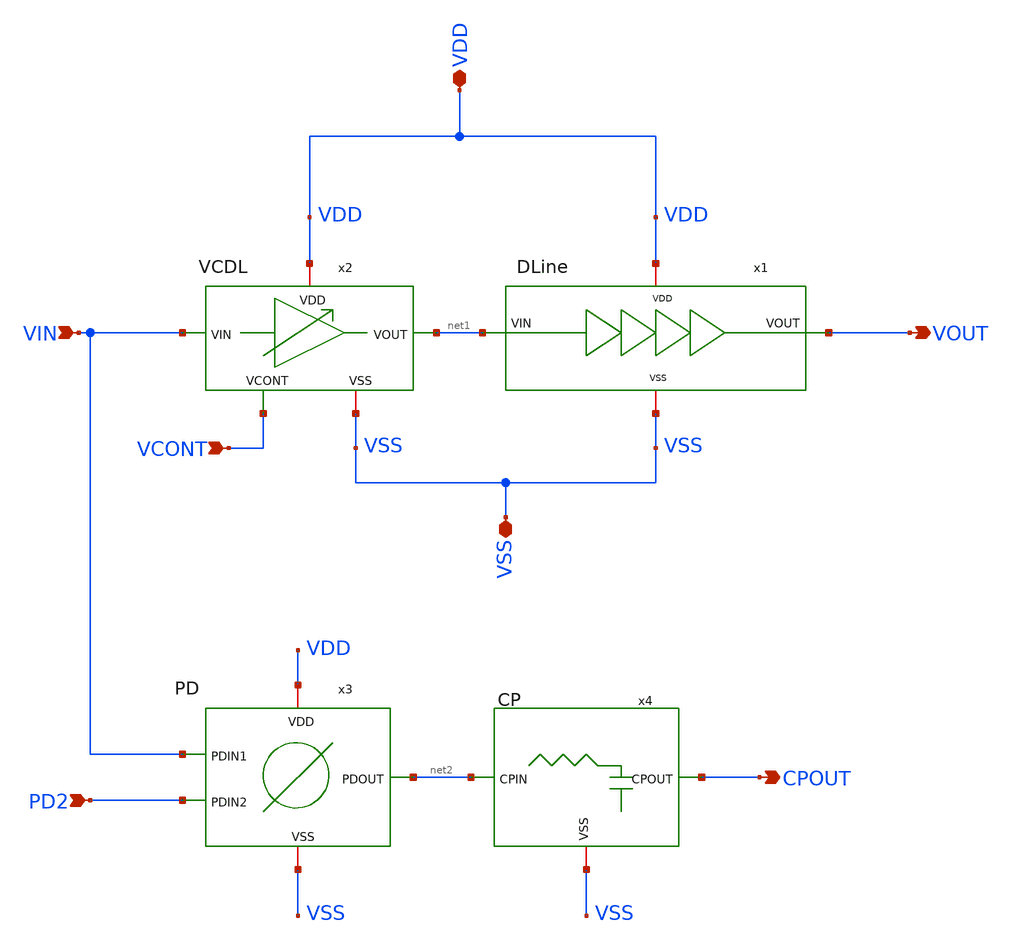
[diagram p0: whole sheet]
** sch_path: Cells/TOP.sch
**.subckt TOP VDD VOUT VCONT VIN VSS PD2 CPOUT
*.iopin VDD
*.opin VOUT
*.ipin VCONT
*.ipin VIN
*.iopin VSS
*.ipin PD2
*.opin CPOUT
x1 VSS VDD net1 VOUT DLine
x2 VDD VIN net1 VCONT VSS VCDL
x3 VDD VSS VIN net2 PD2 PD
x4 net2 CPOUT VSS CP
**.ends
.end
